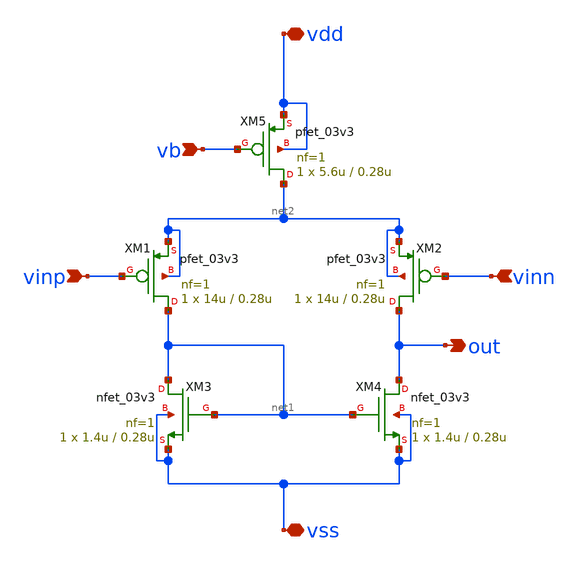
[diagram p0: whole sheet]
** sch_path: opamp/diff-stage.sch
**.subckt diff-stage vinp vinn vb out vdd vss
*.ipin vinp
*.ipin vinn
*.ipin vb
*.opin out
*.iopin vdd
*.iopin vss
XM1 net1 vinp net2 net2 pfet_03v3 L=0.28u W=14u nf=1 ad='int((nf+1)/2) * W/nf * 0.18u' as='int((nf+2)/2) * W/nf * 0.18u'
+ pd='2*int((nf+1)/2) * (W/nf + 0.18u)' ps='2*int((nf+2)/2) * (W/nf + 0.18u)' nrd='0.18u / W' nrs='0.18u / W'
+ sa=0 sb=0 sd=0 m=1
XM2 out vinn net2 net2 pfet_03v3 L=0.28u W=14u nf=1 ad='int((nf+1)/2) * W/nf * 0.18u' as='int((nf+2)/2) * W/nf * 0.18u'
+ pd='2*int((nf+1)/2) * (W/nf + 0.18u)' ps='2*int((nf+2)/2) * (W/nf + 0.18u)' nrd='0.18u / W' nrs='0.18u / W'
+ sa=0 sb=0 sd=0 m=1
XM5 net2 vb vdd vdd pfet_03v3 L=0.28u W=5.6u nf=1 ad='int((nf+1)/2) * W/nf * 0.18u' as='int((nf+2)/2) * W/nf * 0.18u'
+ pd='2*int((nf+1)/2) * (W/nf + 0.18u)' ps='2*int((nf+2)/2) * (W/nf + 0.18u)' nrd='0.18u / W' nrs='0.18u / W'
+ sa=0 sb=0 sd=0 m=1
XM4 out net1 vss vss nfet_03v3 L=0.28u W=1.4u nf=1 ad='int((nf+1)/2) * W/nf * 0.18u' as='int((nf+2)/2) * W/nf * 0.18u'
+ pd='2*int((nf+1)/2) * (W/nf + 0.18u)' ps='2*int((nf+2)/2) * (W/nf + 0.18u)' nrd='0.18u / W' nrs='0.18u / W'
+ sa=0 sb=0 sd=0 m=1
XM3 net1 net1 vss vss nfet_03v3 L=0.28u W=1.4u nf=1 ad='int((nf+1)/2) * W/nf * 0.18u' as='int((nf+2)/2) * W/nf * 0.18u'
+ pd='2*int((nf+1)/2) * (W/nf + 0.18u)' ps='2*int((nf+2)/2) * (W/nf + 0.18u)' nrd='0.18u / W' nrs='0.18u / W'
+ sa=0 sb=0 sd=0 m=1
**.ends
.end
